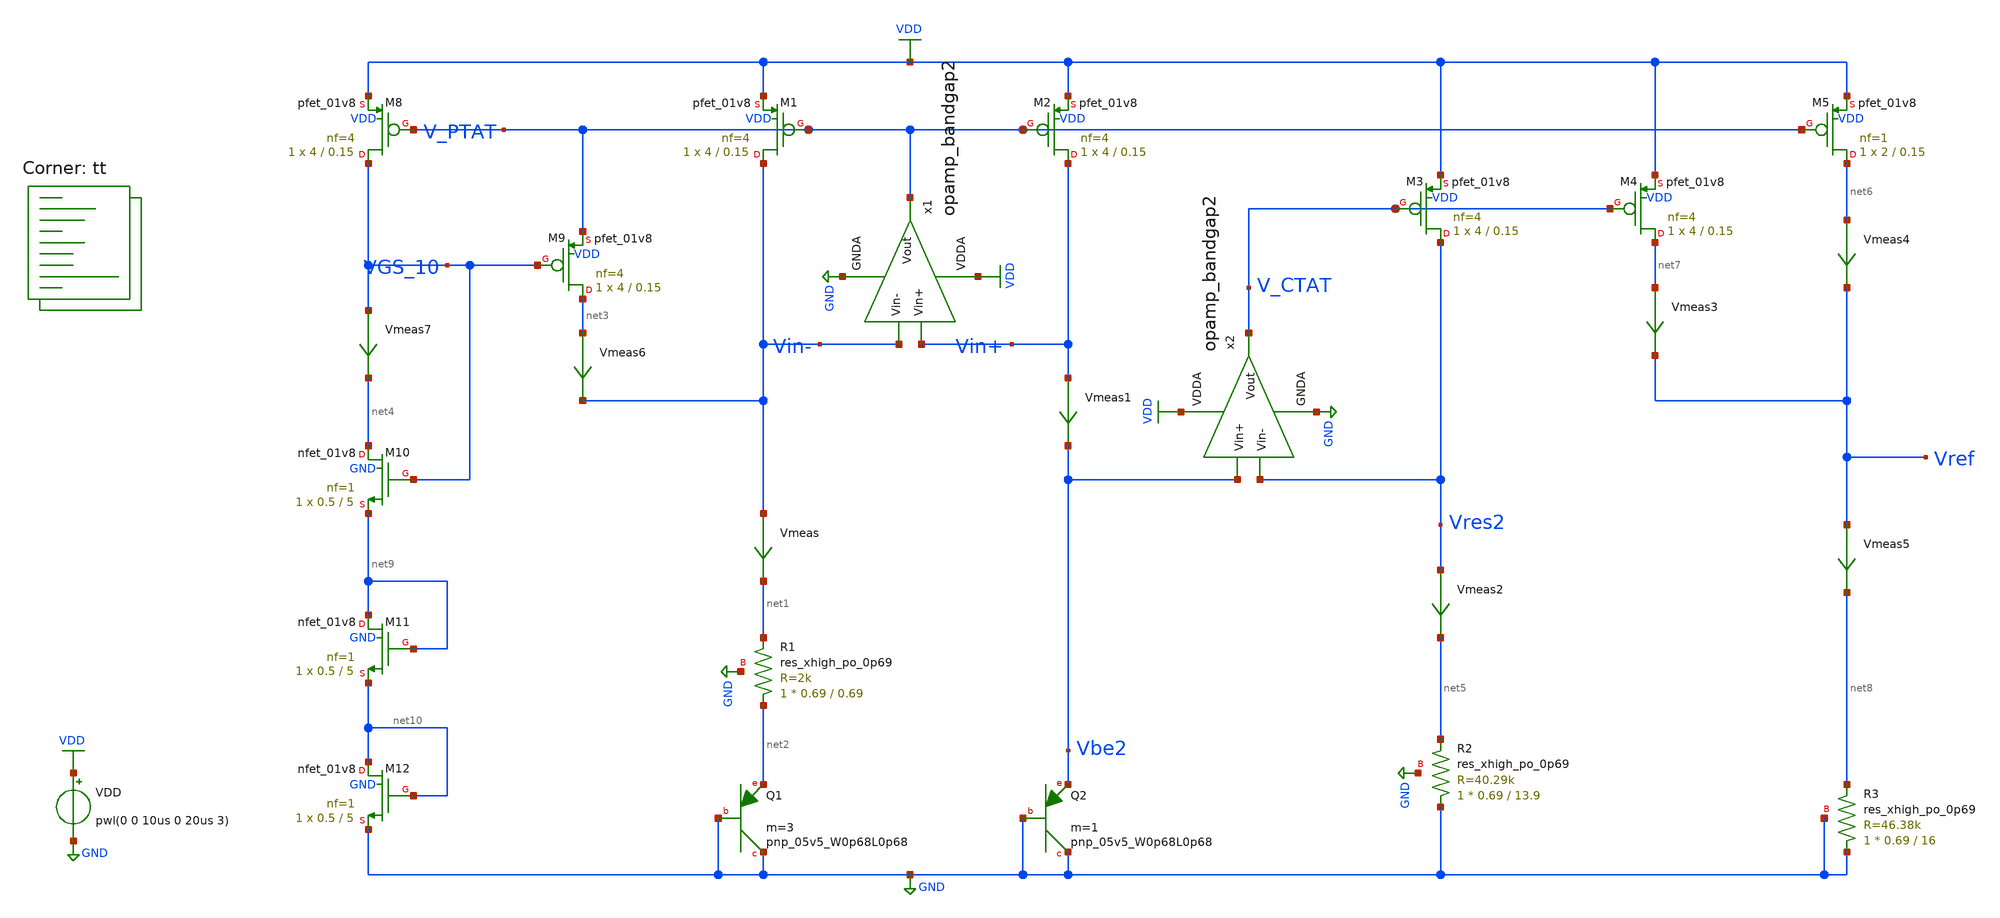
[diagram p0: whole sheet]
** sch_path: projects/bandgapref/xschem_ngspice/old_files/mos_bandgap_baker5.sch
**.subckt mos_bandgap_baker5
VDD VDD GND pwl(0 0 10us 0 20us 3)
Vmeas Vin- net1 0
.save i(vmeas)
Vmeas1 Vin+ Vbe2 0
.save i(vmeas1)
x1 VDD V_PTAT Vin- Vin+ GND opamp_bandgap2
XQ1 GND GND net2 sky130_fd_pr__pnp_05v5_W0p68L0p68 m=3
XQ2 GND GND Vbe2 sky130_fd_pr__pnp_05v5_W0p68L0p68 m=1
XR1 net2 net1 GND sky130_fd_pr__res_xhigh_po_0p69 L=0.69 mult=1 m=1
XM1 Vin- V_PTAT VDD VDD sky130_fd_pr__pfet_01v8 L=0.15 W=4 nf=4 ad='int((nf+1)/2) * W/nf * 0.29' as='int((nf+2)/2) * W/nf * 0.29'
+ pd='2*int((nf+1)/2) * (W/nf + 0.29)' ps='2*int((nf+2)/2) * (W/nf + 0.29)' nrd='0.29 / W' nrs='0.29 / W'
+ sa=0 sb=0 sd=0 mult=1 m=1
XM2 Vin+ V_PTAT VDD VDD sky130_fd_pr__pfet_01v8 L=0.15 W=4 nf=4 ad='int((nf+1)/2) * W/nf * 0.29' as='int((nf+2)/2) * W/nf * 0.29'
+ pd='2*int((nf+1)/2) * (W/nf + 0.29)' ps='2*int((nf+2)/2) * (W/nf + 0.29)' nrd='0.29 / W' nrs='0.29 / W'
+ sa=0 sb=0 sd=0 mult=1 m=1
x2 VDD V_CTAT Vres2 Vbe2 GND opamp_bandgap2
XR2 GND net5 GND sky130_fd_pr__res_xhigh_po_0p69 L=13.9 mult=1 m=1
XM3 Vres2 V_CTAT VDD VDD sky130_fd_pr__pfet_01v8 L=0.15 W=4 nf=4 ad='int((nf+1)/2) * W/nf * 0.29' as='int((nf+2)/2) * W/nf * 0.29'
+ pd='2*int((nf+1)/2) * (W/nf + 0.29)' ps='2*int((nf+2)/2) * (W/nf + 0.29)' nrd='0.29 / W' nrs='0.29 / W'
+ sa=0 sb=0 sd=0 mult=1 m=1
XM4 net7 V_CTAT VDD VDD sky130_fd_pr__pfet_01v8 L=0.15 W=4 nf=4 ad='int((nf+1)/2) * W/nf * 0.29' as='int((nf+2)/2) * W/nf * 0.29'
+ pd='2*int((nf+1)/2) * (W/nf + 0.29)' ps='2*int((nf+2)/2) * (W/nf + 0.29)' nrd='0.29 / W' nrs='0.29 / W'
+ sa=0 sb=0 sd=0 mult=1 m=1
XM5 net6 V_PTAT VDD VDD sky130_fd_pr__pfet_01v8 L=0.15 W=2 nf=1 ad='int((nf+1)/2) * W/nf * 0.29' as='int((nf+2)/2) * W/nf * 0.29'
+ pd='2*int((nf+1)/2) * (W/nf + 0.29)' ps='2*int((nf+2)/2) * (W/nf + 0.29)' nrd='0.29 / W' nrs='0.29 / W'
+ sa=0 sb=0 sd=0 mult=1 m=1
XR3 GND net8 GND sky130_fd_pr__res_xhigh_po_0p69 L=16 mult=1 m=1
XM8 VGS_10 V_PTAT VDD VDD sky130_fd_pr__pfet_01v8 L=0.15 W=4 nf=4 ad='int((nf+1)/2) * W/nf * 0.29' as='int((nf+2)/2) * W/nf * 0.29'
+ pd='2*int((nf+1)/2) * (W/nf + 0.29)' ps='2*int((nf+2)/2) * (W/nf + 0.29)' nrd='0.29 / W' nrs='0.29 / W'
+ sa=0 sb=0 sd=0 mult=1 m=1
XM9 net3 VGS_10 V_PTAT VDD sky130_fd_pr__pfet_01v8 L=0.15 W=4 nf=4 ad='int((nf+1)/2) * W/nf * 0.29' as='int((nf+2)/2) * W/nf * 0.29'
+ pd='2*int((nf+1)/2) * (W/nf + 0.29)' ps='2*int((nf+2)/2) * (W/nf + 0.29)' nrd='0.29 / W' nrs='0.29 / W'
+ sa=0 sb=0 sd=0 mult=1 m=1
XM10 net4 VGS_10 net9 GND sky130_fd_pr__nfet_01v8 L=5 W=0.5 nf=1 ad='int((nf+1)/2) * W/nf * 0.29' as='int((nf+2)/2) * W/nf * 0.29'
+ pd='2*int((nf+1)/2) * (W/nf + 0.29)' ps='2*int((nf+2)/2) * (W/nf + 0.29)' nrd='0.29 / W' nrs='0.29 / W'
+ sa=0 sb=0 sd=0 mult=1 m=1
Vmeas2 Vres2 net5 0
.save i(vmeas2)
Vmeas3 net7 Vref 0
.save i(vmeas3)
Vmeas4 net6 Vref 0
.save i(vmeas4)
Vmeas5 Vref net8 0
.save i(vmeas5)
Vmeas6 net3 Vin- 0
.save i(vmeas6)
Vmeas7 VGS_10 net4 0
.save i(vmeas7)
XM11 net9 net9 net10 GND sky130_fd_pr__nfet_01v8 L=5 W=0.5 nf=1 ad='int((nf+1)/2) * W/nf * 0.29' as='int((nf+2)/2) * W/nf * 0.29'
+ pd='2*int((nf+1)/2) * (W/nf + 0.29)' ps='2*int((nf+2)/2) * (W/nf + 0.29)' nrd='0.29 / W' nrs='0.29 / W'
+ sa=0 sb=0 sd=0 mult=1 m=1
XM12 net10 net10 GND GND sky130_fd_pr__nfet_01v8 L=5 W=0.5 nf=1 ad='int((nf+1)/2) * W/nf * 0.29' as='int((nf+2)/2) * W/nf * 0.29'
+ pd='2*int((nf+1)/2) * (W/nf + 0.29)' ps='2*int((nf+2)/2) * (W/nf + 0.29)' nrd='0.29 / W' nrs='0.29 / W'
+ sa=0 sb=0 sd=0 mult=1 m=1
**** begin user architecture code
.lib $::SKYWATER_MODELS/sky130.lib.spice tt



.option method=gear
.option wnflag=1
.option savecurrents

.save @m.xm1.msky130_fd_pr__pfet_01v8[gm] @m.xm2.msky130_fd_pr__pfet_01v8[gm] @m.xm3.msky130_fd_pr__pfet_01v8[gm] @m.xm4.msky130_fd_pr__pfet_01v8[gm] @m.xm5.msky130_fd_pr__pfet_01v8[gm] @m.xm6.msky130_fd_pr__pfet_01v8[gm] @m.xm7.msky130_fd_pr__pfet_01v8[gm] @m.xm8.msky130_fd_pr__pfet_01v8[gm] @m.xm9.msky130_fd_pr__pfet_01v8[gm] @m.xm10.msky130_fd_pr__nfet_01v8[gm] @m.xm11.msky130_fd_pr__nfet_01v8[gm] @m.xm12.msky130_fd_pr__nfet_01v8[gm]


.control
  save all
  op
  * dc VDD 1.4 3.3 0.1 temp -40 120 1
  tran 1ns 40us
  remzerovec
  write mos_bandgap_baker5.raw
  set appendwrite
.endc




**** end user architecture code
**.ends

* expanding   symbol:
*+  /foss/designs/my_design/projects/pll/bandgapref/xschem_ngspice/opamp_bandgap2.sym # of pins=5
** sym_path: projects/bandgapref/xschem_ngspice/old_files/opamp_bandgap2.sym
** sch_path: projects/bandgapref/xschem_ngspice/old_files/opamp_bandgap2.sch
.subckt opamp_bandgap2 VDDA Vout Vin- Vin+ GNDA
*.ipin Vin+
*.opin Vout
*.ipin Vin-
*.ipin GNDA
*.ipin VDDA
XM2 net2 Vin- net1 GNDA sky130_fd_pr__nfet_01v8 L=0.6 W=2 nf=2 ad='int((nf+1)/2) * W/nf * 0.29' as='int((nf+2)/2) * W/nf * 0.29'
+ pd='2*int((nf+1)/2) * (W/nf + 0.29)' ps='2*int((nf+2)/2) * (W/nf + 0.29)' nrd='0.29 / W' nrs='0.29 / W'
+ sa=0 sb=0 sd=0 mult=1 m=1
XM3 Vout Vin+ net1 GNDA sky130_fd_pr__nfet_01v8 L=0.6 W=2 nf=2 ad='int((nf+1)/2) * W/nf * 0.29' as='int((nf+2)/2) * W/nf * 0.29'
+ pd='2*int((nf+1)/2) * (W/nf + 0.29)' ps='2*int((nf+2)/2) * (W/nf + 0.29)' nrd='0.29 / W' nrs='0.29 / W'
+ sa=0 sb=0 sd=0 mult=1 m=1
XM1 net1 net1 GNDA GNDA sky130_fd_pr__nfet_01v8 L=0.6 W=4 nf=1 ad='int((nf+1)/2) * W/nf * 0.29' as='int((nf+2)/2) * W/nf * 0.29'
+ pd='2*int((nf+1)/2) * (W/nf + 0.29)' ps='2*int((nf+2)/2) * (W/nf + 0.29)' nrd='0.29 / W' nrs='0.29 / W'
+ sa=0 sb=0 sd=0 mult=1 m=1
XM4 Vout net2 VDDA VDDA sky130_fd_pr__pfet_01v8 L=0.6 W=4 nf=4 ad='int((nf+1)/2) * W/nf * 0.29' as='int((nf+2)/2) * W/nf * 0.29'
+ pd='2*int((nf+1)/2) * (W/nf + 0.29)' ps='2*int((nf+2)/2) * (W/nf + 0.29)' nrd='0.29 / W' nrs='0.29 / W'
+ sa=0 sb=0 sd=0 mult=1 m=1
XM5 net2 net2 VDDA VDDA sky130_fd_pr__pfet_01v8 L=0.6 W=4 nf=4 ad='int((nf+1)/2) * W/nf * 0.29' as='int((nf+2)/2) * W/nf * 0.29'
+ pd='2*int((nf+1)/2) * (W/nf + 0.29)' ps='2*int((nf+2)/2) * (W/nf + 0.29)' nrd='0.29 / W' nrs='0.29 / W'
+ sa=0 sb=0 sd=0 mult=1 m=1
.ends

.GLOBAL GND
.GLOBAL VDD
.end
